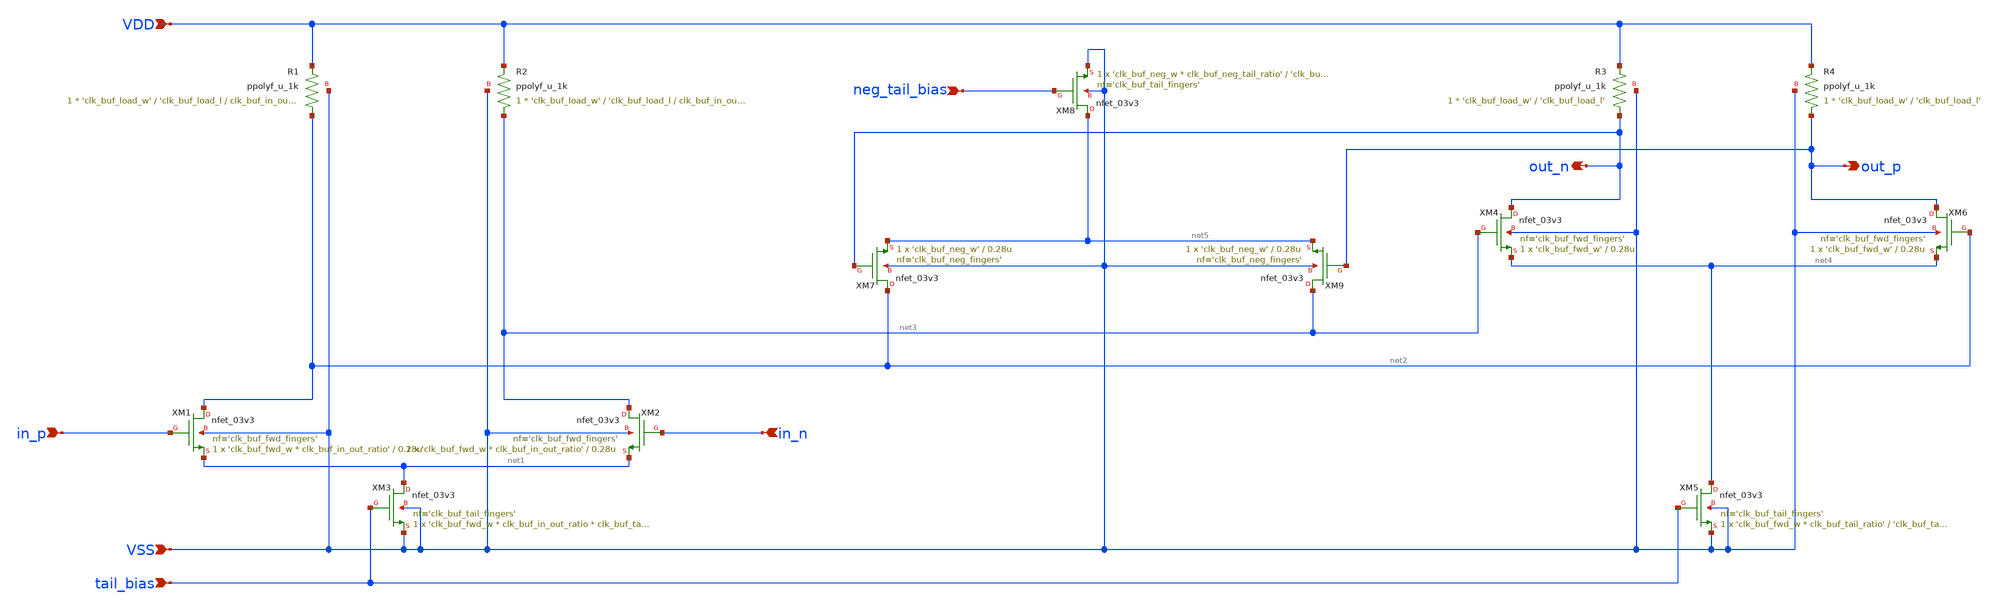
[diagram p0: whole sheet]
** sch_path: xschem/clk_buf.sch
**.subckt clk_buf VSS VDD out_n out_p in_p in_n tail_bias neg_tail_bias
*.ipin VSS
*.ipin VDD
*.opin out_n
*.opin out_p
*.ipin in_p
*.ipin in_n
*.ipin tail_bias
*.ipin neg_tail_bias
XM1 net2 in_p net1 VSS nfet_03v3 L=0.28u W='clk_buf_fwd_w * clk_buf_in_out_ratio' nf='clk_buf_fwd_fingers'
+ ad='int((nf+1)/2) * W/nf * 0.18u' as='int((nf+2)/2) * W/nf * 0.18u' pd='2*int((nf+1)/2) * (W/nf + 0.18u)'
+ ps='2*int((nf+2)/2) * (W/nf + 0.18u)' nrd='0.18u / W' nrs='0.18u / W' sa=0 sb=0 sd=0 m=1
XM3 net1 tail_bias VSS VSS nfet_03v3 L='clk_buf_tail_l' W='clk_buf_fwd_w * clk_buf_in_out_ratio * clk_buf_tail_ratio'
+ nf='clk_buf_tail_fingers' ad='int((nf+1)/2) * W/nf * 0.18u' as='int((nf+2)/2) * W/nf * 0.18u' pd='2*int((nf+1)/2) * (W/nf + 0.18u)'
+ ps='2*int((nf+2)/2) * (W/nf + 0.18u)' nrd='0.18u / W' nrs='0.18u / W' sa=0 sb=0 sd=0 m=1
XM2 net3 in_n net1 VSS nfet_03v3 L=0.28u W='clk_buf_fwd_w * clk_buf_in_out_ratio' nf='clk_buf_fwd_fingers'
+ ad='int((nf+1)/2) * W/nf * 0.18u' as='int((nf+2)/2) * W/nf * 0.18u' pd='2*int((nf+1)/2) * (W/nf + 0.18u)'
+ ps='2*int((nf+2)/2) * (W/nf + 0.18u)' nrd='0.18u / W' nrs='0.18u / W' sa=0 sb=0 sd=0 m=1
XR1 net2 VDD VSS ppolyf_u_1k r_width='clk_buf_load_w' r_length='clk_buf_load_l / clk_buf_in_out_ratio'
+ m=1
XR2 net3 VDD VSS ppolyf_u_1k r_width='clk_buf_load_w' r_length='clk_buf_load_l / clk_buf_in_out_ratio'
+ m=1
XM4 out_n net3 net4 VSS nfet_03v3 L=0.28u W='clk_buf_fwd_w' nf='clk_buf_fwd_fingers' ad='int((nf+1)/2) * W/nf * 0.18u'
+ as='int((nf+2)/2) * W/nf * 0.18u' pd='2*int((nf+1)/2) * (W/nf + 0.18u)' ps='2*int((nf+2)/2) * (W/nf + 0.18u)'
+ nrd='0.18u / W' nrs='0.18u / W' sa=0 sb=0 sd=0 m=1
XM5 net4 tail_bias VSS VSS nfet_03v3 L='clk_buf_tail_l' W='clk_buf_fwd_w * clk_buf_tail_ratio' nf='clk_buf_tail_fingers'
+ ad='int((nf+1)/2) * W/nf * 0.18u' as='int((nf+2)/2) * W/nf * 0.18u' pd='2*int((nf+1)/2) * (W/nf + 0.18u)'
+ ps='2*int((nf+2)/2) * (W/nf + 0.18u)' nrd='0.18u / W' nrs='0.18u / W' sa=0 sb=0 sd=0 m=1
XM6 out_p net2 net4 VSS nfet_03v3 L=0.28u W='clk_buf_fwd_w' nf='clk_buf_fwd_fingers' ad='int((nf+1)/2) * W/nf * 0.18u'
+ as='int((nf+2)/2) * W/nf * 0.18u' pd='2*int((nf+1)/2) * (W/nf + 0.18u)' ps='2*int((nf+2)/2) * (W/nf + 0.18u)'
+ nrd='0.18u / W' nrs='0.18u / W' sa=0 sb=0 sd=0 m=1
XR3 out_n VDD VSS ppolyf_u_1k r_width='clk_buf_load_w' r_length='clk_buf_load_l' m=1
XR4 out_p VDD VSS ppolyf_u_1k r_width='clk_buf_load_w' r_length='clk_buf_load_l' m=1
XM7 net2 out_n net5 VSS nfet_03v3 L=0.28u W='clk_buf_neg_w' nf='clk_buf_neg_fingers' ad='int((nf+1)/2) * W/nf * 0.18u'
+ as='int((nf+2)/2) * W/nf * 0.18u' pd='2*int((nf+1)/2) * (W/nf + 0.18u)' ps='2*int((nf+2)/2) * (W/nf + 0.18u)'
+ nrd='0.18u / W' nrs='0.18u / W' sa=0 sb=0 sd=0 m=1
XM8 net5 neg_tail_bias VSS VSS nfet_03v3 L='clk_buf_tail_l' W='clk_buf_neg_w * clk_buf_neg_tail_ratio'
+ nf='clk_buf_tail_fingers' ad='int((nf+1)/2) * W/nf * 0.18u' as='int((nf+2)/2) * W/nf * 0.18u' pd='2*int((nf+1)/2) * (W/nf + 0.18u)'
+ ps='2*int((nf+2)/2) * (W/nf + 0.18u)' nrd='0.18u / W' nrs='0.18u / W' sa=0 sb=0 sd=0 m=1
XM9 net3 out_p net5 VSS nfet_03v3 L=0.28u W='clk_buf_neg_w' nf='clk_buf_neg_fingers' ad='int((nf+1)/2) * W/nf * 0.18u'
+ as='int((nf+2)/2) * W/nf * 0.18u' pd='2*int((nf+1)/2) * (W/nf + 0.18u)' ps='2*int((nf+2)/2) * (W/nf + 0.18u)'
+ nrd='0.18u / W' nrs='0.18u / W' sa=0 sb=0 sd=0 m=1
**.ends
.end
